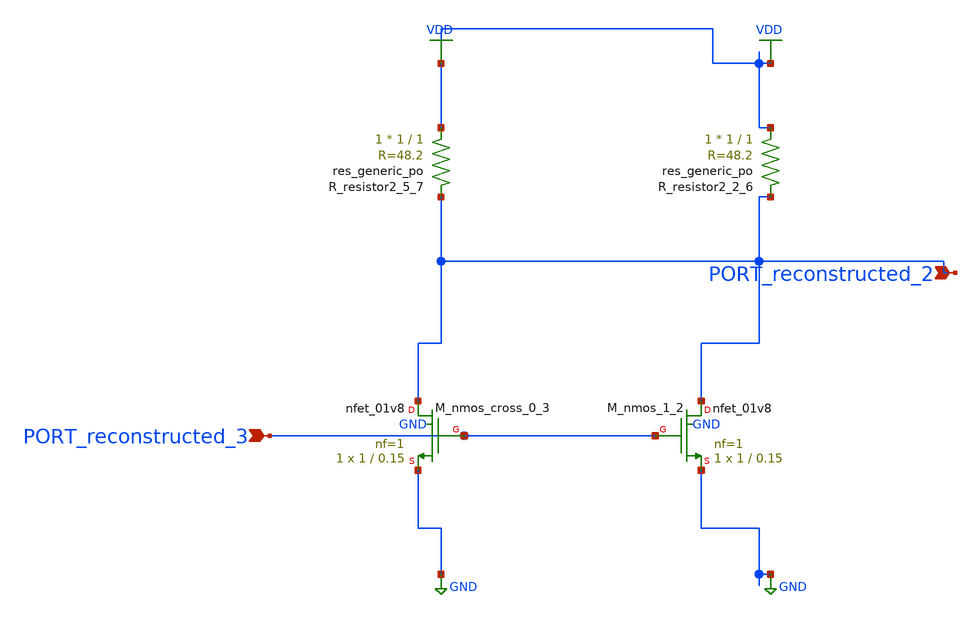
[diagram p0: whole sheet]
** sch_path: schematics/AMSNet/498.sch
**.subckt 498 PORT_reconstructed_2 PORT_reconstructed_3
*.ipin PORT_reconstructed_2
*.ipin PORT_reconstructed_3
XM_nmos_1_2 PORT_reconstructed_2 PORT_reconstructed_3 GND GND sky130_fd_pr__nfet_01v8 L=0.15 W=1 nf=1
+ ad='int((1 + 1)/2) * 1 / 1 * 0.29' as='int((1 + 2)/2) * 1 / 1 * 0.29' pd='2*int((1 + 1)/2) * (1 / 1 + 0.29)'
+ ps='2*int((1 + 2)/2) * (1 / 1 + 0.29)' nrd='0.29 / 1 ' nrs='0.29 / 1 ' sa=0 sb=0 sd=0 mult=1 m=1
XM_nmos_cross_0_3 PORT_reconstructed_2 PORT_reconstructed_3 GND GND sky130_fd_pr__nfet_01v8 L=0.15 W=1
+ nf=1 ad='int((1 + 1)/2) * 1 / 1 * 0.29' as='int((1 + 2)/2) * 1 / 1 * 0.29' pd='2*int((1 + 1)/2) * (1 / 1 + 0.29)'
+ ps='2*int((1 + 2)/2) * (1 / 1 + 0.29)' nrd='0.29 / 1 ' nrs='0.29 / 1 ' sa=0 sb=0 sd=0 mult=1 m=1
XR_resistor2_2_6 VDD PORT_reconstructed_2 sky130_fd_pr__res_generic_po W=1 L=1 m=1
XR_resistor2_5_7 VDD PORT_reconstructed_2 sky130_fd_pr__res_generic_po W=1 L=1 m=1
**.ends
.GLOBAL GND
.GLOBAL VDD
.end
